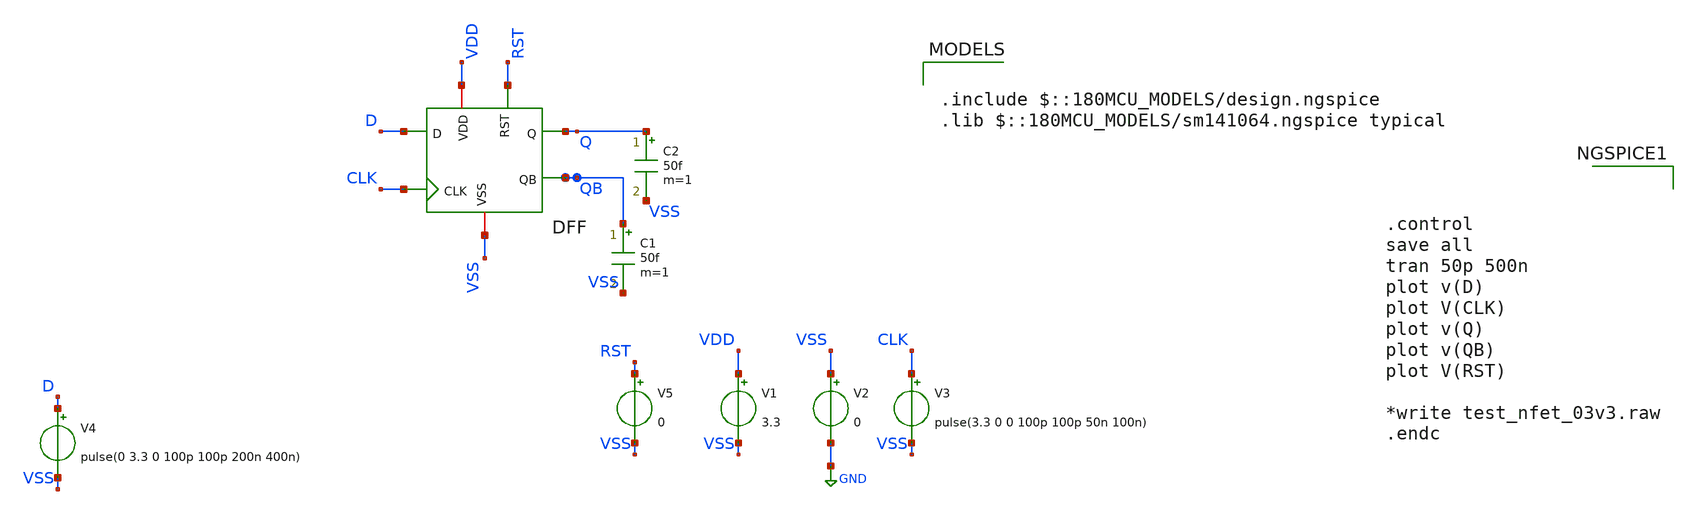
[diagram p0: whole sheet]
** sch_path: Clock_Generator_PAKISTAN_02/Schematics/DFF_test.sch
**.subckt DFF_test
V1 VDD VSS 3.3
V2 VSS GND 0
V3 CLK VSS pulse(3.3 0 0 100p 100p 50n 100n)
V4 D VSS pulse(0 3.3 0 100p 100p 200n 400n)
x1 VSS D RST CLK Q QB VDD DFF
V5 RST VSS 0
C1 QB VSS 50f m=1
C2 Q VSS 50f m=1
**** begin user architecture code

.include $::180MCU_MODELS/design.ngspice
.lib $::180MCU_MODELS/sm141064.ngspice typical




.control
save all
tran 50p 500n
plot v(D)
plot V(CLK)
plot v(Q)
plot v(QB)
plot V(RST)

*write test_nfet_03v3.raw
.endc


**** end user architecture code
**.ends
.GLOBAL GND
.end
